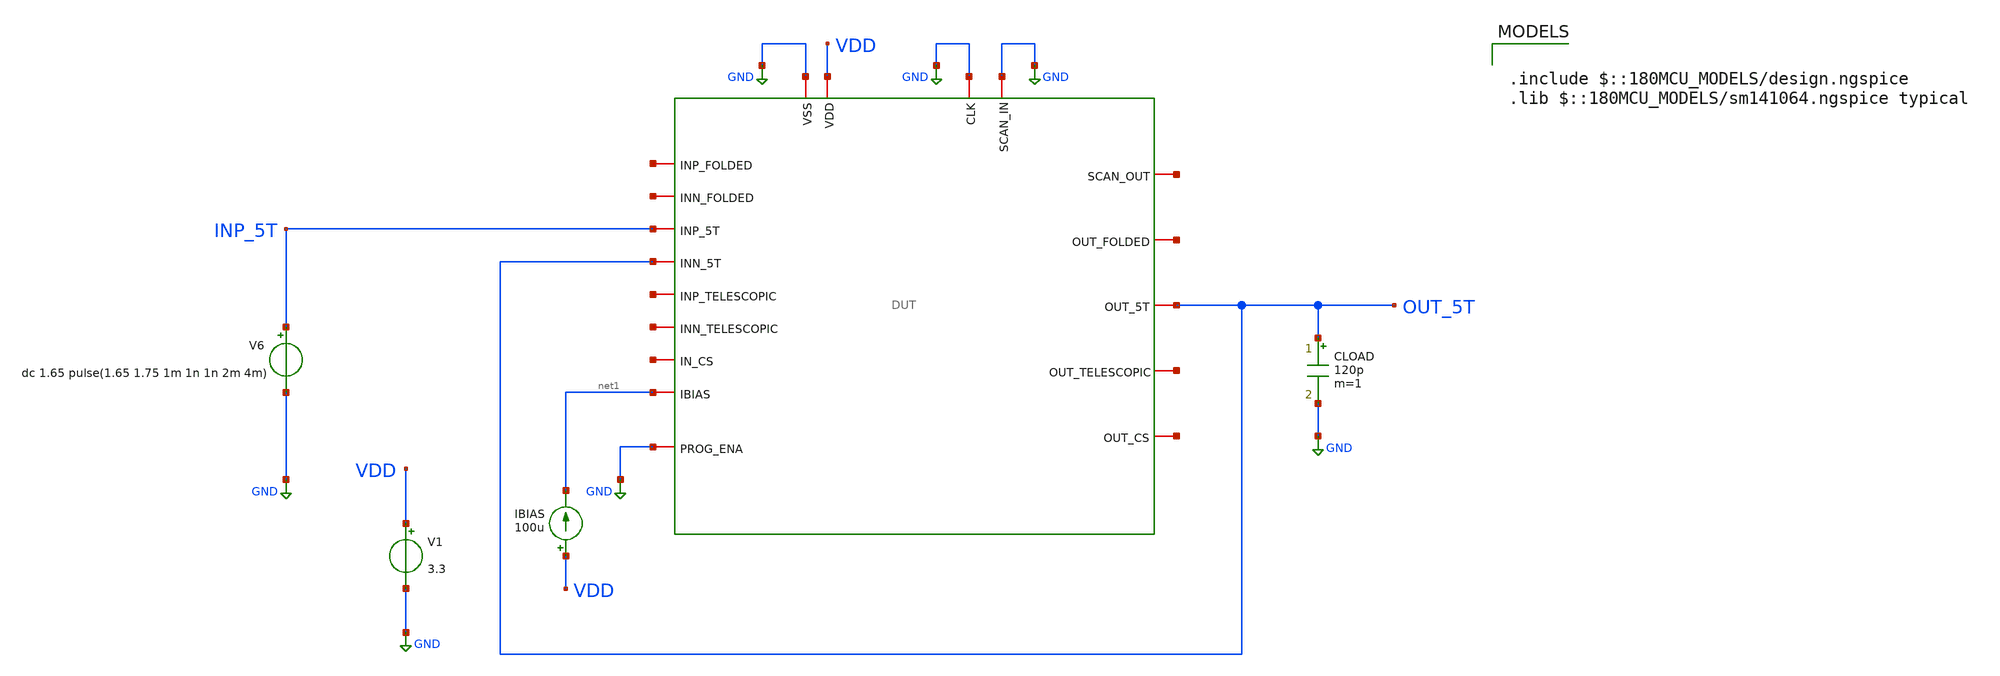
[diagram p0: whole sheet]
** sch_path: designs/libs/pex/5t/step_response/default_step_5t.sch
**.subckt default_step_5t
V1 VDD GND 3.3
CLOAD OUT_5T GND 120p m=1
V6 INP_5T GND dc 1.65 pulse(1.65 1.75 1m 1n 1n 2m 4m)
IBIAS VDD net1 100u
x1 GND net2 GND GND VDD net3 net4 OUT_5T net1 net5 INP_5T OUT_5T net6 net7 net8 net9 net10 GND DUT
**** begin user architecture code

.include $::180MCU_MODELS/design.ngspice
.lib $::180MCU_MODELS/sm141064.ngspice typical



.include /foss/designs/libs/pex/DUT.spice
.control
tran 1u 5m

plot v(out_5t) v(inp_5t)

meas tran v_before find v(out_5t) at=0.99m
meas tran v_after find v(out_5t) at=2.5m

let delta = v_after - v_before
let t20_val = v_before + 0.2 * delta
let t80_val = v_before + 0.8 * delta

meas tran t_20 when v(out_5t) = t20_val rise = 1
meas tran t_80 when v(out_5t) = t80_val rise = 1
let sr_rise = delta / (t_80 - t_20)
print sr_rise

meas tran t_20f when v(out_5t) = t80_val fall = 1
meas tran t_80f when v(out_5t) = t20_val fall = 1
let sr_fall = delta / (t_80f - t_20f)
print sr_fall

meas tran vpeak max v(out_5t) from=1m to=3m
let overshoot = (vpeak - v_after) / delta * 100
print overshoot

meas tran t_settle when v(out_5t) = v_after td = 1m rise = 1
let settling = t_settle - 1m
print settling

print v_before v_after delta
.endc


**** end user architecture code
**.ends
.GLOBAL GND
.end
